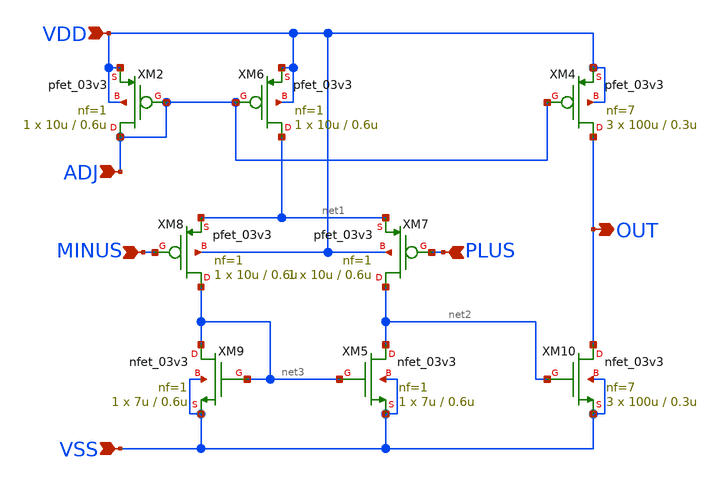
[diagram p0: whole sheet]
** sch_path: macros/Analog/r2r_dac/opamp_chonky.sch
**.subckt opamp_chonky VDD PLUS VSS OUT MINUS ADJ
*.ipin VDD
*.ipin PLUS
*.ipin VSS
*.opin OUT
*.ipin MINUS
*.ipin ADJ
XM4 OUT ADJ VDD VDD pfet_03v3 L=0.3u W=100u nf=7 ad='int((nf+1)/2) * W/nf * 0.18u' as='int((nf+2)/2) * W/nf * 0.18u'
+ pd='2*int((nf+1)/2) * (W/nf + 0.18u)' ps='2*int((nf+2)/2) * (W/nf + 0.18u)' nrd='0.18u / W' nrs='0.18u / W'
+ sa=0 sb=0 sd=0 m=3
XM5 net2 net3 VSS VSS nfet_03v3 L=0.6u W=7u nf=1 ad='int((nf+1)/2) * W/nf * 0.18u' as='int((nf+2)/2) * W/nf * 0.18u'
+ pd='2*int((nf+1)/2) * (W/nf + 0.18u)' ps='2*int((nf+2)/2) * (W/nf + 0.18u)' nrd='0.18u / W' nrs='0.18u / W'
+ sa=0 sb=0 sd=0 m=1
XM6 net1 ADJ VDD VDD pfet_03v3 L=0.6u W=10u nf=1 ad='int((nf+1)/2) * W/nf * 0.18u' as='int((nf+2)/2) * W/nf * 0.18u'
+ pd='2*int((nf+1)/2) * (W/nf + 0.18u)' ps='2*int((nf+2)/2) * (W/nf + 0.18u)' nrd='0.18u / W' nrs='0.18u / W'
+ sa=0 sb=0 sd=0 m=1
XM2 ADJ ADJ VDD VDD pfet_03v3 L=0.6u W=10u nf=1 ad='int((nf+1)/2) * W/nf * 0.18u' as='int((nf+2)/2) * W/nf * 0.18u'
+ pd='2*int((nf+1)/2) * (W/nf + 0.18u)' ps='2*int((nf+2)/2) * (W/nf + 0.18u)' nrd='0.18u / W' nrs='0.18u / W'
+ sa=0 sb=0 sd=0 m=1
XM7 net2 PLUS net1 VDD pfet_03v3 L=0.6u W=10u nf=1 ad='int((nf+1)/2) * W/nf * 0.18u' as='int((nf+2)/2) * W/nf * 0.18u'
+ pd='2*int((nf+1)/2) * (W/nf + 0.18u)' ps='2*int((nf+2)/2) * (W/nf + 0.18u)' nrd='0.18u / W' nrs='0.18u / W'
+ sa=0 sb=0 sd=0 m=1
XM8 net3 MINUS net1 VDD pfet_03v3 L=0.6u W=10u nf=1 ad='int((nf+1)/2) * W/nf * 0.18u' as='int((nf+2)/2) * W/nf * 0.18u'
+ pd='2*int((nf+1)/2) * (W/nf + 0.18u)' ps='2*int((nf+2)/2) * (W/nf + 0.18u)' nrd='0.18u / W' nrs='0.18u / W'
+ sa=0 sb=0 sd=0 m=1
XM9 net3 net3 VSS VSS nfet_03v3 L=0.6u W=7u nf=1 ad='int((nf+1)/2) * W/nf * 0.18u' as='int((nf+2)/2) * W/nf * 0.18u'
+ pd='2*int((nf+1)/2) * (W/nf + 0.18u)' ps='2*int((nf+2)/2) * (W/nf + 0.18u)' nrd='0.18u / W' nrs='0.18u / W'
+ sa=0 sb=0 sd=0 m=1
XM10 OUT net2 VSS VSS nfet_03v3 L=0.3u W=100u nf=7 ad='int((nf+1)/2) * W/nf * 0.18u' as='int((nf+2)/2) * W/nf * 0.18u'
+ pd='2*int((nf+1)/2) * (W/nf + 0.18u)' ps='2*int((nf+2)/2) * (W/nf + 0.18u)' nrd='0.18u / W' nrs='0.18u / W'
+ sa=0 sb=0 sd=0 m=3
**.ends
.end
